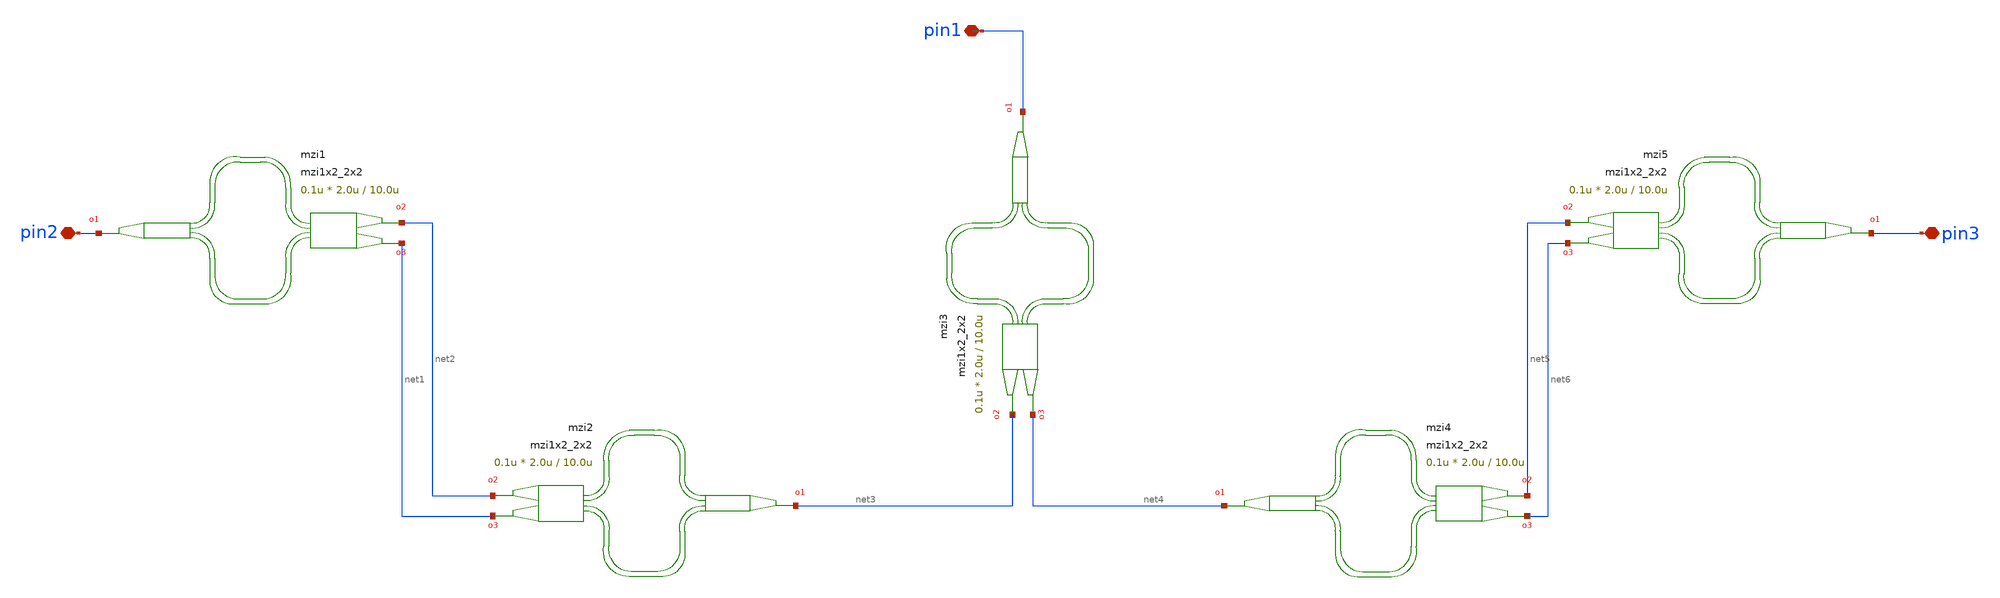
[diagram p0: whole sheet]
** sch_path: xschem/tests/test_sch/test_mzi1x2_2x2.sch
* Copyright (c) 2024, Mabrains LLC
* Licensed under the GNU Lesser General Public License, Version 3.0 (the "License");
* you may not use this file except in compliance with the License.
* GNU Lesser General Public License
* Version 3, 29 June 2007
* This program is free software: you can redistribute it and/or modify
* it under the terms of the GNU Lesser General Public License as published
* by the Free Software Foundation, either version 3 of the License, or
* (at your option) any later version.
* This program is distributed in the hope that it will be useful,
* but WITHOUT ANY WARRANTY; without even the implied warranty of
* MERCHANTABILITY or FITNESS FOR A PARTICULAR PURPOSE.  See the
* GNU Lesser General Public License for more details.
* You should have received a copy of the GNU Lesser General Public License
* along with this program.  If not, see <https://www.gnu.org/licenses/>.
* SPDX-License-Identifier: LGPL-3.0
**.subckt test_mzi1x2_2x2 pin2 pin1 pin3
*.iopin pin2
*.iopin pin1
*.iopin pin3
Pmzi1 pin2 net2 net1 mzi1x2_2x2 delta_length=10.0u length_y=2.0u length_x=0.1u
Pmzi2 net3 net2 net1 mzi1x2_2x2 delta_length=10.0u length_y=2.0u length_x=0.1u
Pmzi3 pin1 net3 net4 mzi1x2_2x2 delta_length=10.0u length_y=2.0u length_x=0.1u
Pmzi4 net4 net5 net6 mzi1x2_2x2 delta_length=10.0u length_y=2.0u length_x=0.1u
Pmzi5 pin3 net5 net6 mzi1x2_2x2 delta_length=10.0u length_y=2.0u length_x=0.1u
**.ends
.end
